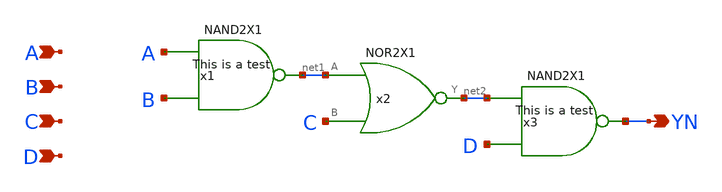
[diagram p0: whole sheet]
** sch_path: archives/lib/xschem/AOAI4X1.sch
**.subckt AOAI4X1 YN A B C D
*.opin YN
*.ipin A
*.ipin B
*.ipin C
*.ipin D
x1 net1 A B VDD VSS NAND2X1
x2 net2 net1 C VDD VSS NOR2X1
x3 YN net2 D VDD VSS NAND2X1
**.ends
.end
